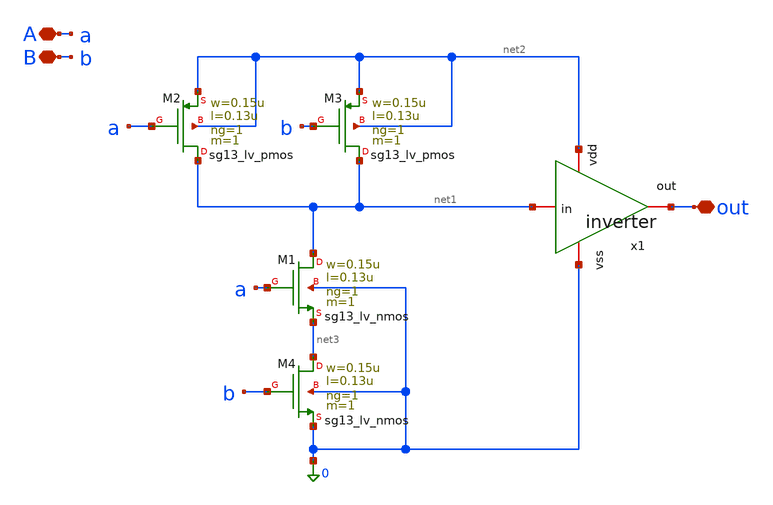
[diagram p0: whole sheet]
** sch_path: design/blocks/compuerta_and.sch
**.subckt compuerta_and A B out
*.iopin A
*.iopin B
*.iopin out
XM2 net1 a net2 net2 sg13_lv_pmos w=0.15u l=0.13u ng=1 m=1 mm_ok=1
XM1 net1 a net3 0 sg13_lv_nmos w=0.15u l=0.13u ng=1 m=1 mm_ok=1
XM3 net1 b net2 net2 sg13_lv_pmos w=0.15u l=0.13u ng=1 m=1 mm_ok=1
XM4 net3 b 0 0 sg13_lv_nmos w=0.15u l=0.13u ng=1 m=1 mm_ok=1
x1 net2 out net1 0 inverter
**.ends

* expanding   symbol:  blocks/inverter/schematic/inverter.sym # of pins=4
** sym_path: design/blocks/inverter/schematic/inverter.sym
** sch_path: design/blocks/inverter/schematic/inverter.sch
.subckt inverter vdd out in vss
*.iopin vdd
*.iopin out
*.iopin vss
*.iopin in
XM1 out in vss vss sg13_lv_nmos w=0.15u l=0.13u ng=1 m=1 mm_ok=1
XM2 out in vdd vdd sg13_lv_pmos w=0.3u l=0.13u ng=1 m=1 mm_ok=1
.ends

.end
